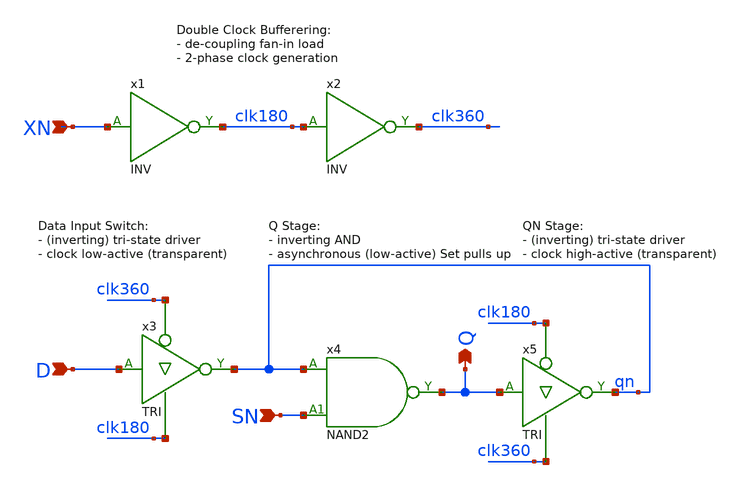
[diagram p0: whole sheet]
** sch_path: Sources/crafted/LATNS.sch
**.subckt LATNS XN D Q SN
*.ipin XN
*.ipin D
*.opin Q
*.ipin SN
x4 qn SN Q VDD GND NAND2 Wmin=1.5u Lmin=1u g=2 m=1
x3 D clk360 clk180 qn VDD GND TRI Wmin=1.5u Lmin=1u g=2 m=1
x5 Q clk180 clk360 qn VDD GND TRI Wmin=1.5u Lmin=1u g=2 m=1
x1 XN clk180 VDD GND INV Wmin=1.5u Lmin=1u g=2 m=1
x2 clk180 clk360 VDD GND INV Wmin=1.5u Lmin=1u g=2 m=1
**.ends
.end
